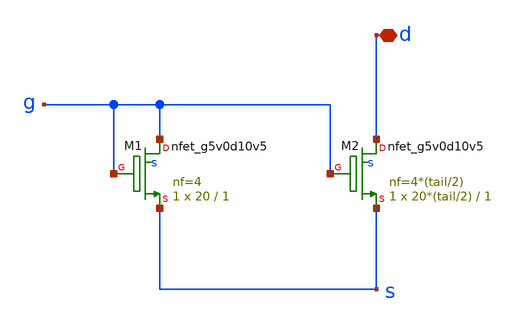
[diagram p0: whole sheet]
** sch_path: xschem/mosbius_lib/mosbius_ntail.sch
**.subckt mosbius_ntail d
*.iopin d
XM1 g g s s sky130_fd_pr__nfet_g5v0d10v5 L=1 W=20 nf=4 ad='int((nf+1)/2) * W/nf * 0.29' as='int((nf+2)/2) * W/nf * 0.29'
+ pd='2*int((nf+1)/2) * (W/nf + 0.29)' ps='2*int((nf+2)/2) * (W/nf + 0.29)' nrd='0.29 / W' nrs='0.29 / W'
+ sa=0 sb=0 sd=0 mult=1 m=1
XM2 d g s s sky130_fd_pr__nfet_g5v0d10v5 L=1 W=20*(tail/2) nf=4*(tail/2) ad='int((nf+1)/2) * W/nf * 0.29'
+ as='int((nf+2)/2) * W/nf * 0.29' pd='2*int((nf+1)/2) * (W/nf + 0.29)' ps='2*int((nf+2)/2) * (W/nf + 0.29)'
+ nrd='0.29 / W' nrs='0.29 / W' sa=0 sb=0 sd=0 mult=1 m=1
**.ends
.end
